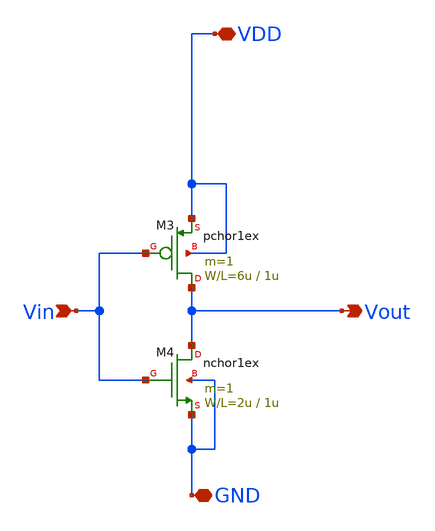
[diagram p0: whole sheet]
** sch_path: member_project/SHOTARO-TOMOOKA/tomooka.sch
**.subckt tomooka VDD GND Vin Vout
*.iopin VDD
*.iopin GND
*.ipin Vin
*.opin Vout
M3 Vout Vin VDD VDD pchor1ex L=1u W=6u m=1
M4 Vout Vin GND GND nchor1ex L=1u W=2u m=1
**.ends
.end
